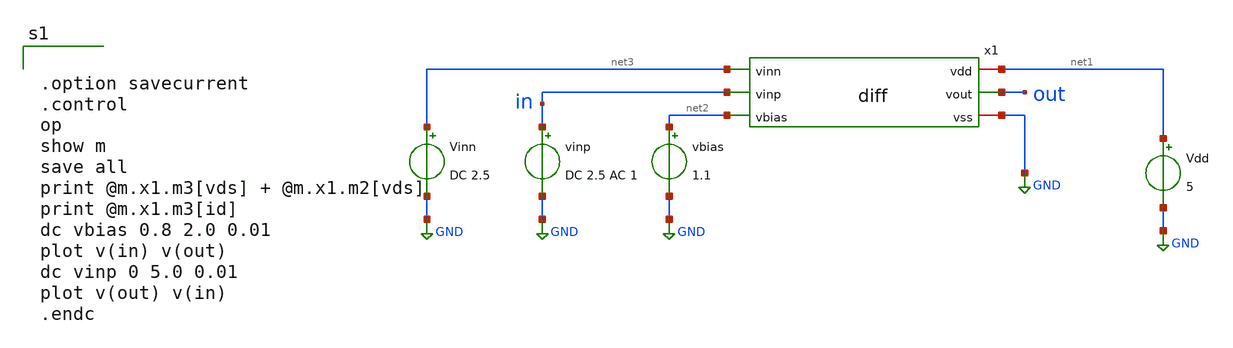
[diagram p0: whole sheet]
** sch_path: member_project/GroupWork/Team_masahiro/diff_dc.sch
**.subckt diff_dc
x1 net1 out net3 in net2 GND diff
Vinn net3 GND DC 2.5
vinp in GND DC 2.5 AC 1
vbias net2 GND 1.1
Vdd net1 GND 5
**** begin user architecture code
 .include $::LIB/mos.lib
.include $::LIB/passive.lib
.include $::LIB/diode.lib


.option savecurrent
.control
op
show m
save all
print @m.x1.m3[vds] + @m.x1.m2[vds]
print @m.x1.m3[id]
dc vbias 0.8 2.0 0.01
plot v(in) v(out)
dc vinp 0 5.0 0.01
plot v(out) v(in)
.endc


**** end user architecture code
**.ends

* expanding   symbol:  diff.sym # of pins=6
** sym_path: member_project/GroupWork/Team_masahiro/diff.sym
** sch_path: member_project/GroupWork/Team_masahiro/diff.sch
.subckt diff vdd vout vinn vinp vbias vss
*.iopin vss
*.iopin vdd
*.ipin vinn
*.ipin vinp
*.opin vout
*.ipin vbias
M1 net1 vinn net2 vss nmos L=2u W=100u m=1
M2 vout vinp net2 vss nmos L=2u W=100u m=1
M3 net2 vbias vss vss nmos L=2u W=20u m=1
M4 net1 net1 vdd vdd pmos L=2u W=35u m=1
M5 vout net1 vdd vdd pmos L=2u W=35u m=1
.ends

.GLOBAL GND
.end
